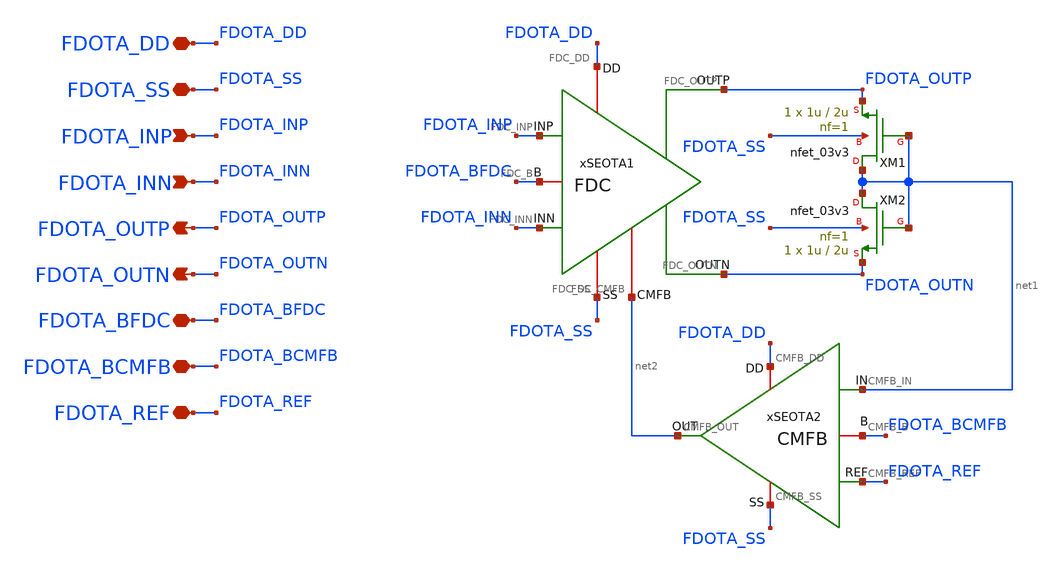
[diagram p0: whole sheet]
** sch_path: Design_Files/IC Design/Schematic/FD_OTA/FDOTA/FD_OTA.sch
**.subckt FD_OTA FDOTA_DD FDOTA_SS FDOTA_INP FDOTA_INN FDOTA_OUTP FDOTA_BFDC FDOTA_OUTN FDOTA_BCMFB
*+ FDOTA_REF
*.iopin FDOTA_DD
*.iopin FDOTA_SS
*.ipin FDOTA_INP
*.ipin FDOTA_INN
*.opin FDOTA_OUTP
*.iopin FDOTA_BFDC
*.opin FDOTA_OUTN
*.iopin FDOTA_BCMFB
*.iopin FDOTA_REF
xSEOTA1 FDOTA_DD FDOTA_SS FDOTA_INP FDOTA_INN FDOTA_OUTN FDOTA_BFDC FDOTA_OUTP net2 FDC
xSEOTA2 FDOTA_DD FDOTA_SS net1 FDOTA_REF net2 FDOTA_BCMFB CMFB
XM1 net1 net1 FDOTA_OUTP FDOTA_SS nfet_03v3 L=2u W=1u nf=1 ad='int((nf+1)/2) * W/nf * 0.18u' as='int((nf+2)/2) * W/nf * 0.18u'
+ pd='2*int((nf+1)/2) * (W/nf + 0.18u)' ps='2*int((nf+2)/2) * (W/nf + 0.18u)' nrd='0.18u / W' nrs='0.18u / W'
+ sa=0 sb=0 sd=0 m=1
XM2 net1 net1 FDOTA_OUTN FDOTA_SS nfet_03v3 L=2u W=1u nf=1 ad='int((nf+1)/2) * W/nf * 0.18u' as='int((nf+2)/2) * W/nf * 0.18u'
+ pd='2*int((nf+1)/2) * (W/nf + 0.18u)' ps='2*int((nf+2)/2) * (W/nf + 0.18u)' nrd='0.18u / W' nrs='0.18u / W'
+ sa=0 sb=0 sd=0 m=1
**.ends

* expanding   symbol:  ECG_Acquisition_IC/Design_Files/IC Design/Schematic/FD_OTA/FDC/FDC.sym # of
*+ pins=8
** sym_path: Design_Files/IC Design/Schematic/FD_OTA/FDC/FDC.sym
** sch_path: Design_Files/IC Design/Schematic/FD_OTA/FDC/FDC.sch
.subckt FDC FDC_DD FDC_SS FDC_INP FDC_INN FDC_OUTN FDC_B FDC_OUTP FDC_CMFB
*.iopin FDC_DD
*.iopin FDC_SS
*.ipin FDC_INP
*.ipin FDC_INN
*.opin FDC_OUTP
*.iopin FDC_B
*.opin FDC_OUTN
*.iopin FDC_CMFB
XM3 net4 FDC_CMFB FDC_DD FDC_DD pfet_03v3 L=2u W=1u nf=1 ad='int((nf+1)/2) * W/nf * 0.18u' as='int((nf+2)/2) * W/nf * 0.18u'
+ pd='2*int((nf+1)/2) * (W/nf + 0.18u)' ps='2*int((nf+2)/2) * (W/nf + 0.18u)' nrd='0.18u / W' nrs='0.18u / W'
+ sa=0 sb=0 sd=0 m=200
XM8 FDC_OUTP FDC_B FDC_SS FDC_SS nfet_03v3 L=0.5u W=1u nf=1 ad='int((nf+1)/2) * W/nf * 0.18u' as='int((nf+2)/2) * W/nf * 0.18u'
+ pd='2*int((nf+1)/2) * (W/nf + 0.18u)' ps='2*int((nf+2)/2) * (W/nf + 0.18u)' nrd='0.18u / W' nrs='0.18u / W'
+ sa=0 sb=0 sd=0 m=120
Rz net1 net2 2k m=1
XM5 net3 FDC_B FDC_SS FDC_SS nfet_03v3 L=2u W=1u nf=1 ad='int((nf+1)/2) * W/nf * 0.18u' as='int((nf+2)/2) * W/nf * 0.18u'
+ pd='2*int((nf+1)/2) * (W/nf + 0.18u)' ps='2*int((nf+2)/2) * (W/nf + 0.18u)' nrd='0.18u / W' nrs='0.18u / W'
+ sa=0 sb=0 sd=0 m=20
XM6 FDC_OUTP net1 FDC_DD FDC_DD pfet_03v3 L=0.5u W=1u nf=1 ad='int((nf+1)/2) * W/nf * 0.18u' as='int((nf+2)/2) * W/nf * 0.18u'
+ pd='2*int((nf+1)/2) * (W/nf + 0.18u)' ps='2*int((nf+2)/2) * (W/nf + 0.18u)' nrd='0.18u / W' nrs='0.18u / W'
+ sa=0 sb=0 sd=0 m=400
XM10 FDC_B FDC_B FDC_SS FDC_SS nfet_03v3 L=2u W=1u nf=1 ad='int((nf+1)/2) * W/nf * 0.18u' as='int((nf+2)/2) * W/nf * 0.18u'
+ pd='2*int((nf+1)/2) * (W/nf + 0.18u)' ps='2*int((nf+2)/2) * (W/nf + 0.18u)' nrd='0.18u / W' nrs='0.18u / W'
+ sa=0 sb=0 sd=0 m=50
Cc net2 FDC_OUTP 2p m=1
XM9 FDC_OUTN FDC_B FDC_SS FDC_SS nfet_03v3 L=0.5u W=1u nf=1 ad='int((nf+1)/2) * W/nf * 0.18u' as='int((nf+2)/2) * W/nf * 0.18u'
+ pd='2*int((nf+1)/2) * (W/nf + 0.18u)' ps='2*int((nf+2)/2) * (W/nf + 0.18u)' nrd='0.18u / W' nrs='0.18u / W'
+ sa=0 sb=0 sd=0 m=120
Rz1 net4 net5 2k m=1
XM7 FDC_OUTN net4 FDC_DD FDC_DD pfet_03v3 L=0.5u W=1u nf=1 ad='int((nf+1)/2) * W/nf * 0.18u' as='int((nf+2)/2) * W/nf * 0.18u'
+ pd='2*int((nf+1)/2) * (W/nf + 0.18u)' ps='2*int((nf+2)/2) * (W/nf + 0.18u)' nrd='0.18u / W' nrs='0.18u / W'
+ sa=0 sb=0 sd=0 m=400
Cc1 net5 FDC_OUTN 2p m=1
XM4 net1 FDC_CMFB FDC_DD FDC_DD pfet_03v3 L=2u W=1u nf=1 ad='int((nf+1)/2) * W/nf * 0.18u' as='int((nf+2)/2) * W/nf * 0.18u'
+ pd='2*int((nf+1)/2) * (W/nf + 0.18u)' ps='2*int((nf+2)/2) * (W/nf + 0.18u)' nrd='0.18u / W' nrs='0.18u / W'
+ sa=0 sb=0 sd=0 m=200
XM1 net4 FDC_INN net3 FDC_SS nfet_03v3 L=2u W=1u nf=1 ad='int((nf+1)/2) * W/nf * 0.18u' as='int((nf+2)/2) * W/nf * 0.18u'
+ pd='2*int((nf+1)/2) * (W/nf + 0.18u)' ps='2*int((nf+2)/2) * (W/nf + 0.18u)' nrd='0.18u / W' nrs='0.18u / W'
+ sa=0 sb=0 sd=0 m=400
XM2 net1 FDC_INP net3 FDC_SS nfet_03v3 L=2u W=1u nf=1 ad='int((nf+1)/2) * W/nf * 0.18u' as='int((nf+2)/2) * W/nf * 0.18u'
+ pd='2*int((nf+1)/2) * (W/nf + 0.18u)' ps='2*int((nf+2)/2) * (W/nf + 0.18u)' nrd='0.18u / W' nrs='0.18u / W'
+ sa=0 sb=0 sd=0 m=400
.ends


* expanding   symbol:  ECG_Acquisition_IC/Design_Files/IC Design/Schematic/FD_OTA/CMFB/CMFB.sym # of
*+ pins=6
** sym_path: Design_Files/IC Design/Schematic/FD_OTA/CMFB/CMFB.sym
** sch_path: Design_Files/IC Design/Schematic/FD_OTA/CMFB/CMFB.sch
.subckt CMFB CMFB_DD CMFB_SS CMFB_IN CMFB_REF CMFB_OUT CMFB_B
*.iopin CMFB_DD
*.iopin CMFB_SS
*.ipin CMFB_IN
*.ipin CMFB_REF
*.opin CMFB_OUT
*.iopin CMFB_B
XM4 CMFB_OUT net2 CMFB_DD CMFB_DD pfet_03v3 L=1u W=1u nf=1 ad='int((nf+1)/2) * W/nf * 0.18u' as='int((nf+2)/2) * W/nf * 0.18u'
+ pd='2*int((nf+1)/2) * (W/nf + 0.18u)' ps='2*int((nf+2)/2) * (W/nf + 0.18u)' nrd='0.18u / W' nrs='0.18u / W'
+ sa=0 sb=0 sd=0 m=100
XM3 net2 net2 CMFB_DD CMFB_DD pfet_03v3 L=1u W=1u nf=1 ad='int((nf+1)/2) * W/nf * 0.18u' as='int((nf+2)/2) * W/nf * 0.18u'
+ pd='2*int((nf+1)/2) * (W/nf + 0.18u)' ps='2*int((nf+2)/2) * (W/nf + 0.18u)' nrd='0.18u / W' nrs='0.18u / W'
+ sa=0 sb=0 sd=0 m=100
XM1 net2 CMFB_REF net1 CMFB_SS nfet_03v3 L=1u W=1u nf=1 ad='int((nf+1)/2) * W/nf * 0.18u' as='int((nf+2)/2) * W/nf * 0.18u'
+ pd='2*int((nf+1)/2) * (W/nf + 0.18u)' ps='2*int((nf+2)/2) * (W/nf + 0.18u)' nrd='0.18u / W' nrs='0.18u / W'
+ sa=0 sb=0 sd=0 m=100
XM2 CMFB_OUT CMFB_IN net1 CMFB_SS nfet_03v3 L=1u W=1u nf=1 ad='int((nf+1)/2) * W/nf * 0.18u' as='int((nf+2)/2) * W/nf * 0.18u'
+ pd='2*int((nf+1)/2) * (W/nf + 0.18u)' ps='2*int((nf+2)/2) * (W/nf + 0.18u)' nrd='0.18u / W' nrs='0.18u / W'
+ sa=0 sb=0 sd=0 m=100
XM5 net1 CMFB_B CMFB_SS CMFB_SS nfet_03v3 L=1u W=1u nf=1 ad='int((nf+1)/2) * W/nf * 0.18u' as='int((nf+2)/2) * W/nf * 0.18u'
+ pd='2*int((nf+1)/2) * (W/nf + 0.18u)' ps='2*int((nf+2)/2) * (W/nf + 0.18u)' nrd='0.18u / W' nrs='0.18u / W'
+ sa=0 sb=0 sd=0 m=20
XM10 CMFB_B CMFB_B CMFB_SS CMFB_SS nfet_03v3 L=1u W=1u nf=1 ad='int((nf+1)/2) * W/nf * 0.18u' as='int((nf+2)/2) * W/nf * 0.18u'
+ pd='2*int((nf+1)/2) * (W/nf + 0.18u)' ps='2*int((nf+2)/2) * (W/nf + 0.18u)' nrd='0.18u / W' nrs='0.18u / W'
+ sa=0 sb=0 sd=0 m=50
.ends

.end
